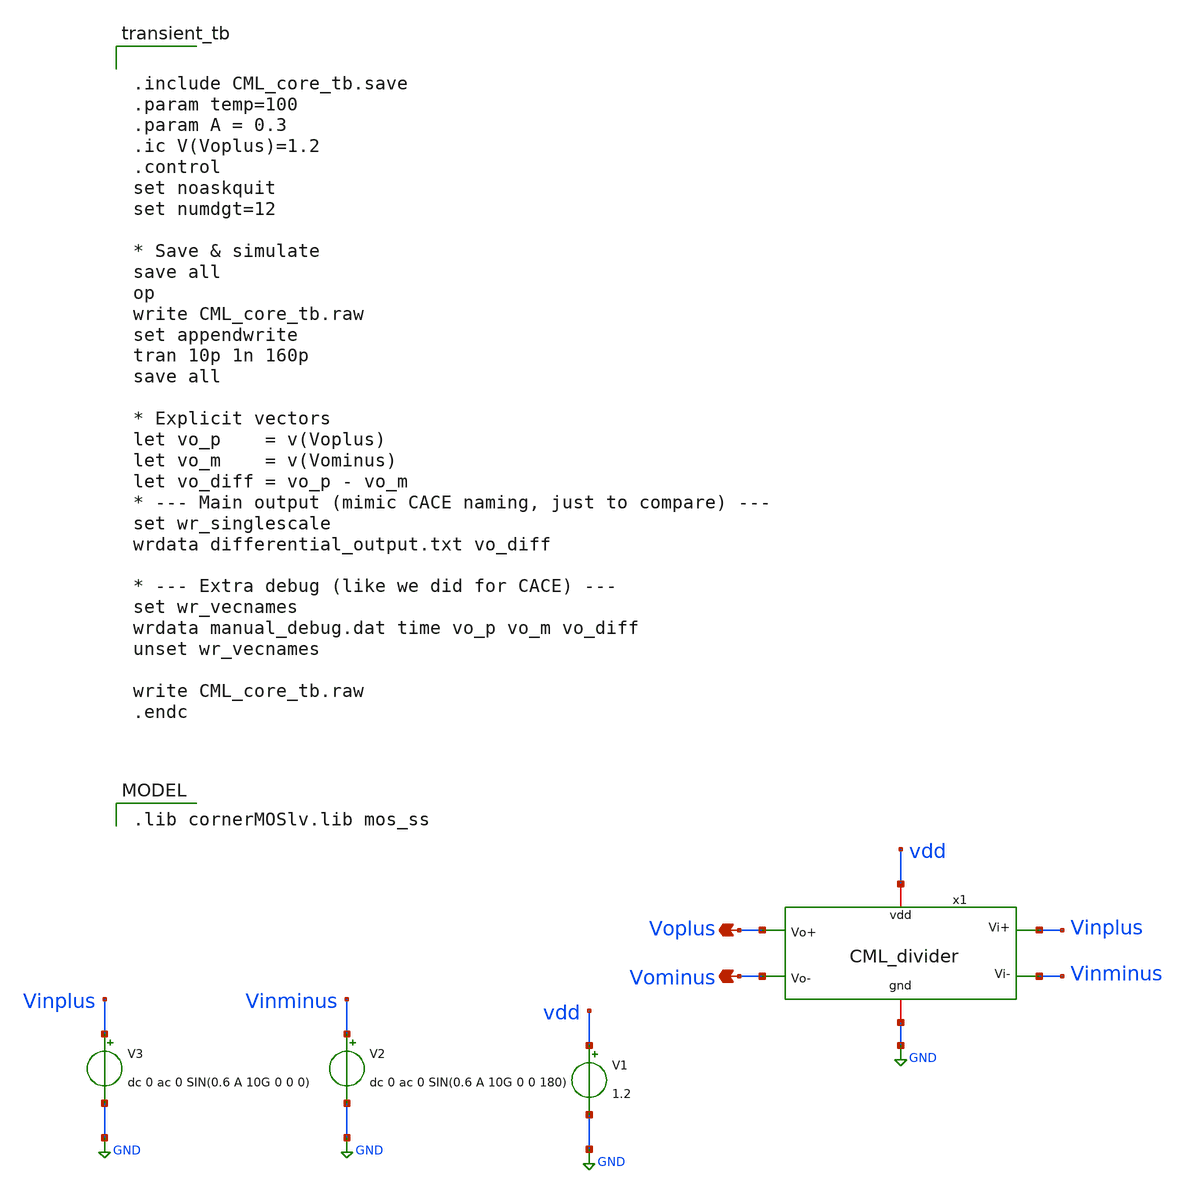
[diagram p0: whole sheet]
** sch_path: modules/module_4_type_2_PLL/CML_divider/testbench/CML_core_tb.sch
**.subckt CML_core_tb Voplus Vominus
*.opin Voplus
*.opin Vominus
V1 vdd GND 1.2
V3 Vinplus GND dc 0 ac 0 SIN(0.6 A 10G 0 0 0)
V2 Vinminus GND dc 0 ac 0 SIN(0.6 A 10G 0 0 180)
x1 Voplus Vominus Vinplus Vinminus vdd GND CML_divider
**** begin user architecture code


.include CML_core_tb.save
.param temp=100
.param A = 0.3
.ic V(Voplus)=1.2
.control
set noaskquit
set numdgt=12

* Save & simulate
save all
op
write CML_core_tb.raw
set appendwrite
tran 10p 1n 160p
save all

* Explicit vectors
let vo_p    = v(Voplus)
let vo_m    = v(Vominus)
let vo_diff = vo_p - vo_m
* --- Main output (mimic CACE naming, just to compare) ---
set wr_singlescale
wrdata differential_output.txt vo_diff

* --- Extra debug (like we did for CACE) ---
set wr_vecnames
wrdata manual_debug.dat time vo_p vo_m vo_diff
unset wr_vecnames

write CML_core_tb.raw
.endc


 .lib cornerMOSlv.lib mos_ss

**** end user architecture code
**.ends

* expanding   symbol:  CML_divider.sym # of pins=6
** sym_path: modules/module_4_type_2_PLL/CML_divider/xschem/CML_divider.sym
** sch_path: modules/module_4_type_2_PLL/CML_divider/xschem/CML_divider.sch
.subckt CML_divider Vo+ Vo- Vi+ Vi- vdd gnd
*.ipin Vi+
*.ipin Vi-
*.opin Vo-
*.iopin vdd
*.iopin gnd
*.opin Vo+
XM1 net2 Vo+ net1 gnd sg13_lv_nmos w=2u l=0.13u ng=1 m=1 mm_ok=1
XM2 net3 Vo- net1 gnd sg13_lv_nmos w=2u l=0.13u ng=1 m=1 mm_ok=1
R1 vdd net2 2.5k m=1
R2 vdd net3 2.5k m=1
XM3 net1 Vi+ net4 gnd sg13_lv_nmos w=2u l=0.2u ng=1 m=1 mm_ok=1
I0 net4 gnd 200u
XM4 net5 Vi- net4 gnd sg13_lv_nmos w=2u l=0.2u ng=1 m=1 mm_ok=1
XM5 net3 net2 net5 gnd sg13_lv_nmos w=2u l=0.13u ng=1 m=1 mm_ok=1
XM6 net2 net3 net5 gnd sg13_lv_nmos w=2u l=0.13u ng=1 m=1 mm_ok=1
XM7 Vo- net2 net6 gnd sg13_lv_nmos w=2u l=0.13u ng=1 m=1 mm_ok=1
XM8 Vo+ net3 net6 gnd sg13_lv_nmos w=2u l=0.13u ng=1 m=1 mm_ok=1
R3 vdd Vo- 2.5k m=1
R4 vdd Vo+ 2.5k m=1
XM9 net6 Vi- net7 gnd sg13_lv_nmos w=2u l=0.2u ng=1 m=1 mm_ok=1
I1 net7 gnd 200u
XM10 net8 Vi+ net7 gnd sg13_lv_nmos w=2u l=0.2u ng=1 m=1 mm_ok=1
XM11 Vo+ Vo- net8 gnd sg13_lv_nmos w=2u l=0.13u ng=1 m=1 mm_ok=1
XM12 Vo- Vo+ net8 gnd sg13_lv_nmos w=2u l=0.13u ng=1 m=1 mm_ok=1
.ends

.GLOBAL GND
.end
